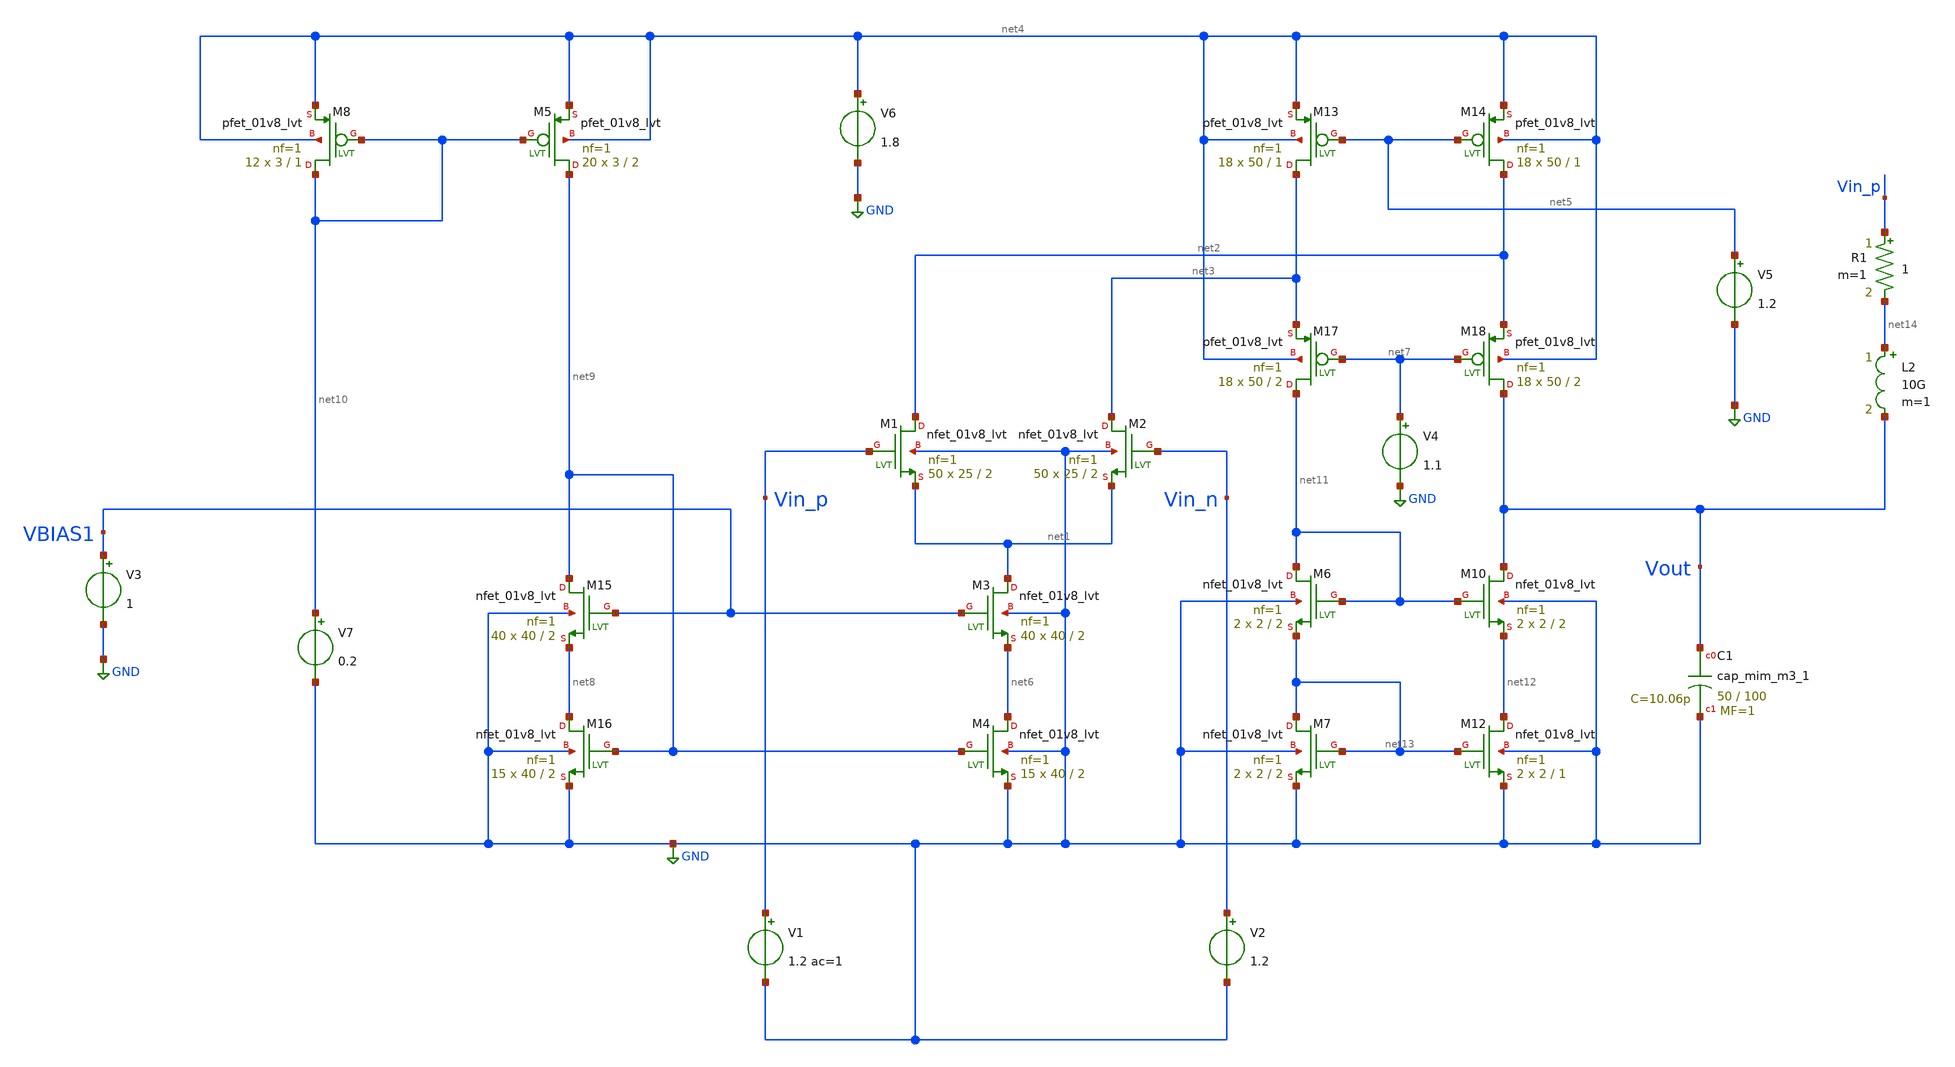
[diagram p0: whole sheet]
** sch_path: xschem/ip_block/opamp/folded_cas_xiaoyi/OTA-2.0.sch
**.subckt OTA-2.0
XM1 net2 Vin_p net1 GND sky130_fd_pr__nfet_01v8_lvt L=2 W=25 nf=1 ad='int((nf+1)/2) * W/nf * 0.29' as='int((nf+2)/2) * W/nf * 0.29'
+ pd='2*int((nf+1)/2) * (W/nf + 0.29)' ps='2*int((nf+2)/2) * (W/nf + 0.29)' nrd='0.29 / W' nrs='0.29 / W'
+ sa=0 sb=0 sd=0 mult=50 m=50
XM2 net3 Vin_n net1 GND sky130_fd_pr__nfet_01v8_lvt L=2 W=25 nf=1 ad='int((nf+1)/2) * W/nf * 0.29' as='int((nf+2)/2) * W/nf * 0.29'
+ pd='2*int((nf+1)/2) * (W/nf + 0.29)' ps='2*int((nf+2)/2) * (W/nf + 0.29)' nrd='0.29 / W' nrs='0.29 / W'
+ sa=0 sb=0 sd=0 mult=50 m=50
XM3 net1 VBIAS1 net6 GND sky130_fd_pr__nfet_01v8_lvt L=2 W=40 nf=1 ad='int((nf+1)/2) * W/nf * 0.29' as='int((nf+2)/2) * W/nf * 0.29'
+ pd='2*int((nf+1)/2) * (W/nf + 0.29)' ps='2*int((nf+2)/2) * (W/nf + 0.29)' nrd='0.29 / W' nrs='0.29 / W'
+ sa=0 sb=0 sd=0 mult=40 m=40
XM4 net6 net9 GND GND sky130_fd_pr__nfet_01v8_lvt L=2 W=40 nf=1 ad='int((nf+1)/2) * W/nf * 0.29' as='int((nf+2)/2) * W/nf * 0.29'
+ pd='2*int((nf+1)/2) * (W/nf + 0.29)' ps='2*int((nf+2)/2) * (W/nf + 0.29)' nrd='0.29 / W' nrs='0.29 / W'
+ sa=0 sb=0 sd=0 mult=15 m=15
XM10 Vout net11 net12 GND sky130_fd_pr__nfet_01v8_lvt L=2 W=2 nf=1 ad='int((nf+1)/2) * W/nf * 0.29' as='int((nf+2)/2) * W/nf * 0.29'
+ pd='2*int((nf+1)/2) * (W/nf + 0.29)' ps='2*int((nf+2)/2) * (W/nf + 0.29)' nrd='0.29 / W' nrs='0.29 / W'
+ sa=0 sb=0 sd=0 mult=2 m=2
XM12 net12 net13 GND GND sky130_fd_pr__nfet_01v8_lvt L=1 W=2 nf=1 ad='int((nf+1)/2) * W/nf * 0.29' as='int((nf+2)/2) * W/nf * 0.29'
+ pd='2*int((nf+1)/2) * (W/nf + 0.29)' ps='2*int((nf+2)/2) * (W/nf + 0.29)' nrd='0.29 / W' nrs='0.29 / W'
+ sa=0 sb=0 sd=0 mult=2 m=2
V2 Vin_n GND 1.2
XM15 net9 VBIAS1 net8 GND sky130_fd_pr__nfet_01v8_lvt L=2 W=40 nf=1 ad='int((nf+1)/2) * W/nf * 0.29'
+ as='int((nf+2)/2) * W/nf * 0.29' pd='2*int((nf+1)/2) * (W/nf + 0.29)' ps='2*int((nf+2)/2) * (W/nf + 0.29)'
+ nrd='0.29 / W' nrs='0.29 / W' sa=0 sb=0 sd=0 mult=40 m=40
XM16 net8 net9 GND GND sky130_fd_pr__nfet_01v8_lvt L=2 W=40 nf=1 ad='int((nf+1)/2) * W/nf * 0.29' as='int((nf+2)/2) * W/nf * 0.29'
+ pd='2*int((nf+1)/2) * (W/nf + 0.29)' ps='2*int((nf+2)/2) * (W/nf + 0.29)' nrd='0.29 / W' nrs='0.29 / W'
+ sa=0 sb=0 sd=0 mult=15 m=15
V3 VBIAS1 GND 1
V6 net4 GND 1.8
XM8 net10 net10 net4 net4 sky130_fd_pr__pfet_01v8_lvt L=1 W=3 nf=1 ad='int((nf+1)/2) * W/nf * 0.29' as='int((nf+2)/2) * W/nf * 0.29'
+ pd='2*int((nf+1)/2) * (W/nf + 0.29)' ps='2*int((nf+2)/2) * (W/nf + 0.29)' nrd='0.29 / W' nrs='0.29 / W'
+ sa=0 sb=0 sd=0 mult=12 m=12
XM5 net9 net10 net4 net4 sky130_fd_pr__pfet_01v8_lvt L=2 W=3 nf=1 ad='int((nf+1)/2) * W/nf * 0.29' as='int((nf+2)/2) * W/nf * 0.29'
+ pd='2*int((nf+1)/2) * (W/nf + 0.29)' ps='2*int((nf+2)/2) * (W/nf + 0.29)' nrd='0.29 / W' nrs='0.29 / W'
+ sa=0 sb=0 sd=0 mult=20 m=20
XM13 net3 net5 net4 net4 sky130_fd_pr__pfet_01v8_lvt L=1 W=50 nf=1 ad='int((nf+1)/2) * W/nf * 0.29' as='int((nf+2)/2) * W/nf * 0.29'
+ pd='2*int((nf+1)/2) * (W/nf + 0.29)' ps='2*int((nf+2)/2) * (W/nf + 0.29)' nrd='0.29 / W' nrs='0.29 / W'
+ sa=0 sb=0 sd=0 mult=18 m=18
XM14 net2 net5 net4 net4 sky130_fd_pr__pfet_01v8_lvt L=1 W=50 nf=1 ad='int((nf+1)/2) * W/nf * 0.29' as='int((nf+2)/2) * W/nf * 0.29'
+ pd='2*int((nf+1)/2) * (W/nf + 0.29)' ps='2*int((nf+2)/2) * (W/nf + 0.29)' nrd='0.29 / W' nrs='0.29 / W'
+ sa=0 sb=0 sd=0 mult=18 m=18
XM17 net11 net7 net3 net4 sky130_fd_pr__pfet_01v8_lvt L=2 W=50 nf=1 ad='int((nf+1)/2) * W/nf * 0.29'
+ as='int((nf+2)/2) * W/nf * 0.29' pd='2*int((nf+1)/2) * (W/nf + 0.29)' ps='2*int((nf+2)/2) * (W/nf + 0.29)'
+ nrd='0.29 / W' nrs='0.29 / W' sa=0 sb=0 sd=0 mult=18 m=18
XM18 Vout net7 net2 net4 sky130_fd_pr__pfet_01v8_lvt L=2 W=50 nf=1 ad='int((nf+1)/2) * W/nf * 0.29' as='int((nf+2)/2) * W/nf * 0.29'
+ pd='2*int((nf+1)/2) * (W/nf + 0.29)' ps='2*int((nf+2)/2) * (W/nf + 0.29)' nrd='0.29 / W' nrs='0.29 / W'
+ sa=0 sb=0 sd=0 mult=18 m=18
XC1 Vout GND sky130_fd_pr__cap_mim_m3_1 W=50 L=100 MF=1 m=1
V4 net7 GND 1.1
V5 net5 GND 1.2
V7 net10 GND 0.2
V1 Vin_p GND 1.2 ac=1
L2 net14 Vout 10G m=1
R1 Vin_p net14 1 m=1
XM6 net11 net11 net13 GND sky130_fd_pr__nfet_01v8_lvt L=2 W=2 nf=1 ad='int((nf+1)/2) * W/nf * 0.29' as='int((nf+2)/2) * W/nf * 0.29'
+ pd='2*int((nf+1)/2) * (W/nf + 0.29)' ps='2*int((nf+2)/2) * (W/nf + 0.29)' nrd='0.29 / W' nrs='0.29 / W'
+ sa=0 sb=0 sd=0 mult=2 m=2
XM7 net13 net13 GND GND sky130_fd_pr__nfet_01v8_lvt L=2 W=2 nf=1 ad='int((nf+1)/2) * W/nf * 0.29' as='int((nf+2)/2) * W/nf * 0.29'
+ pd='2*int((nf+1)/2) * (W/nf + 0.29)' ps='2*int((nf+2)/2) * (W/nf + 0.29)' nrd='0.29 / W' nrs='0.29 / W'
+ sa=0 sb=0 sd=0 mult=2 m=2
**** begin user architecture code


.option temp=70

.op
.ac dec 10 1 1G
*.tran 0.1n 100u

.control
ac dec 10 1 1G
*tran 0.1n 100u
*ac dec 10 1 1G
let phase = 180/PI*vp(Vout)

plot vdb(Vout) phase
*plot Vin_p Vout
.endc

.save all




** opencircuitdesign pdks install
.lib $::SKYWATER_MODELS/sky130.lib.spice tt


**** end user architecture code
**.ends
.GLOBAL GND
.end
